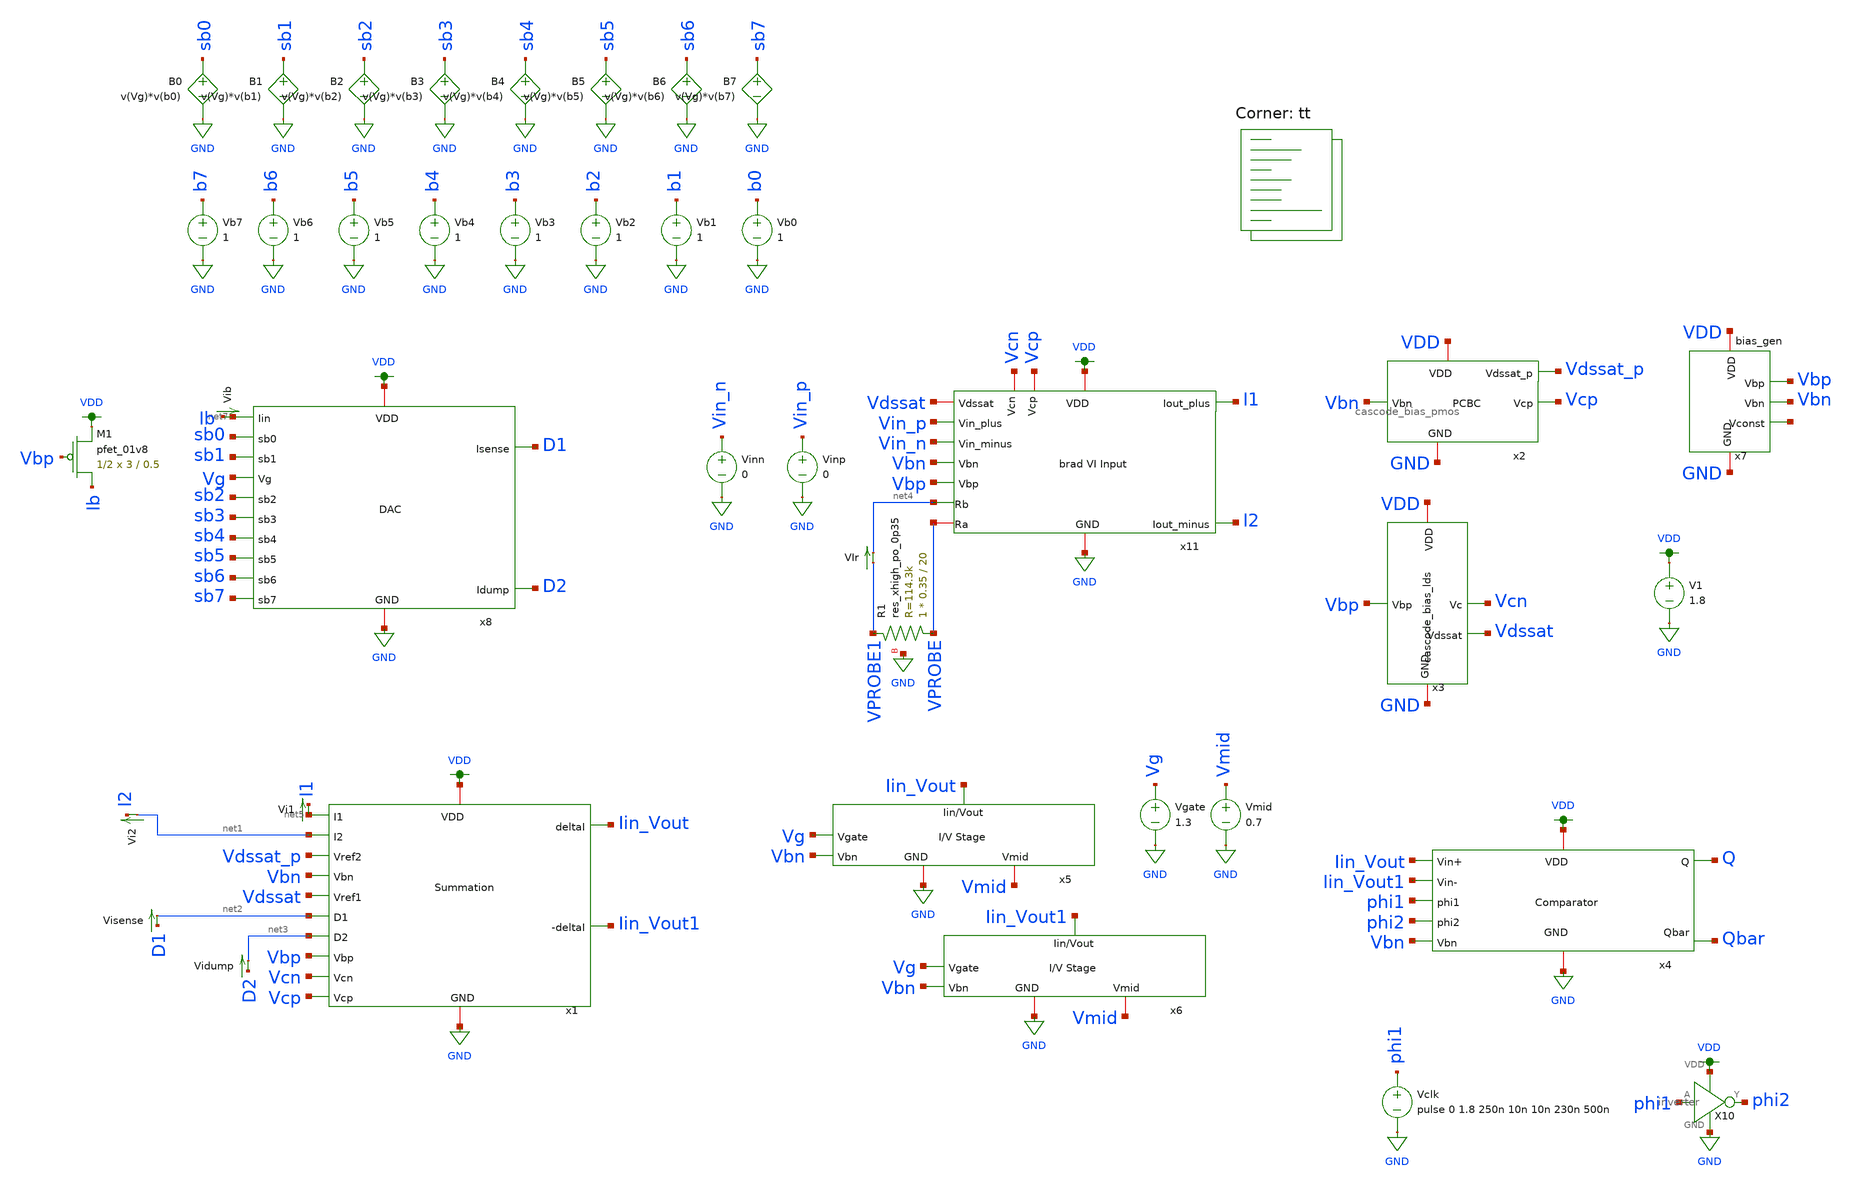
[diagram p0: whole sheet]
** sch_path: final/schematics/adc_tb_1.sch
**.subckt adc_tb_1
x1 VDD GND net5 net1 Vdssat_p Vbn Vdssat net2 net3 Iin_Vout Iin_Vout1 Vbp Vcn Vcp summation
x2 Vbn VDD GND Vcp Vdssat_p cascode_bias_pmos
x3 Vbp VDD Vcn GND Vdssat cascode_bias_lds
V1 VDD GND 1.8
x5 Iin_Vout Vg Vmid Vbn GND IV_converter
x6 Iin_Vout1 Vg Vmid Vbn GND IV_converter
Vgate Vg GND 1.3
Vmid Vmid GND 0.7
x7 VDD Vbp net6 GND Vbn bias_gen
Vidump D2 net3 0
.save i(vidump)
Visense D1 net2 0
.save i(visense)
Vi2 net1 I2 0
.save i(vi2)
Vi1 net5 I1 0
.save i(vi1)
x4 VDD Vbn Iin_Vout Iin_Vout1 phi1 phi2 Q Qbar GND comparator
X10 VDD phi1 phi2 GND inverter
Vclk phi1 GND pulse 0 1.8 250n 10n 10n 230n 500n
x8 sb0 VDD GND sb1 Vg sb2 sb3 D1 sb4 D2 sb5 sb6 sb7 net7 dac
Vb0 b0 GND 1
B0 sb0 GND V=v(Vg)*v(b0)
Vb1 b1 GND 1
B1 sb1 GND V=v(Vg)*v(b1)
Vb2 b2 GND 1
B2 sb2 GND V=v(Vg)*v(b2)
Vb3 b3 GND 1
B3 sb3 GND V=v(Vg)*v(b3)
Vb4 b4 GND 1
B4 sb4 GND V=v(Vg)*v(b4)
Vb5 b5 GND 1
B5 sb5 GND V=v(Vg)*v(b5)
Vb6 b6 GND 1
B6 sb6 GND V=v(Vg)*v(b6)
Vb7 b7 GND 1
B7 sb7 GND V=v(Vg)*v(b7)
XM1 Ib Vbp VDD VDD sky130_fd_pr__pfet_01v8 L=0.5 W=3 nf=1 ad='int((nf+1)/2) * W/nf * 0.29' as='int((nf+2)/2) * W/nf * 0.29'
+ pd='2*int((nf+1)/2) * (W/nf + 0.29)' ps='2*int((nf+2)/2) * (W/nf + 0.29)' nrd='0.29 / W' nrs='0.29 / W'
+ sa=0 sb=0 sd=0 mult=1/2 m=1/2
Vib Ib net7 0
.save i(vib)
Vinp Vin_p GND 0
Vinn Vin_n GND 0
x11 VDD I1 I2 Vin_p Vin_n Vbn Vbp Vcn GND VPROBE net4 Vdssat Vcp brad_VI_input
VIr VPROBE1 net4 0
.save i(vir)
XR1 VPROBE VPROBE1 GND sky130_fd_pr__res_xhigh_po_0p35 L=20 mult=1 m=1
**** begin user architecture code
.lib $::SKYWATER_MODELS/sky130.lib.spice tt


.control
  let mc_runs = 1
  let run = 1
  dowhile run <= mc_runs
    set wr_vecnames
    set appendwrite = FALSE
    set wr_singlescale
    let code = 0
    while code < 256
      if code eq 0
        let b0 = 0
      else
        let b0 = code % 2
      end
      if floor(code / 2) eq 0
        let b1 = 0
      else
        let b1 = floor(code / 2) % 2
      end
      if floor(code / 4) eq 0
        let b2 = 0
      else
        let b2 = floor(code / 4) % 2
      end
      if floor(code / 8) eq 0
        let b3 = 0
      else
        let b3 = floor(code / 8) % 2
      end
      if floor(code / 16) eq 0
        let b4 = 0
      else
        let b4 = floor(code / 16) % 2
      end
      if floor(code / 32) eq 0
        let b5 = 0
      else
        let b5 = floor(code / 32) % 2
      end
      if floor(code / 64) eq 0
        let b6 = 0
      else
        let b6 = floor(code / 64) % 2
      end
      if floor(code / 128) eq 0
        let b7 = 0
      else
        let b7 = floor(code / 128) % 2
      end
      alter vb0 $&b0
      alter vb1 $&b1
      alter vb2 $&b2
      alter vb3 $&b3
      alter vb4 $&b4
      alter vb5 $&b5
      alter vb6 $&b6
      alter vb7 $&b7
      save all
      op
      wrdata ~/Documents/madvlsi/final/schematics/adctest/adc_tb{$&run}.txt code v(sb0) v(sb1) v(sb2)
+ v(sb3) v(sb4) v(sb5) v(sb6) v(sb7) i(vib) i(visense) i(vidump) v(q) v(qbar)
      if code eq 0
        set appendwrite
        set wr_vecnames = FALSE
      end
      let code = code + 1
    end
    reset
    let run = run + 1
  end
quit
.endc

**** end user architecture code
**.ends
.GLOBAL VDD
.GLOBAL GND
.end
